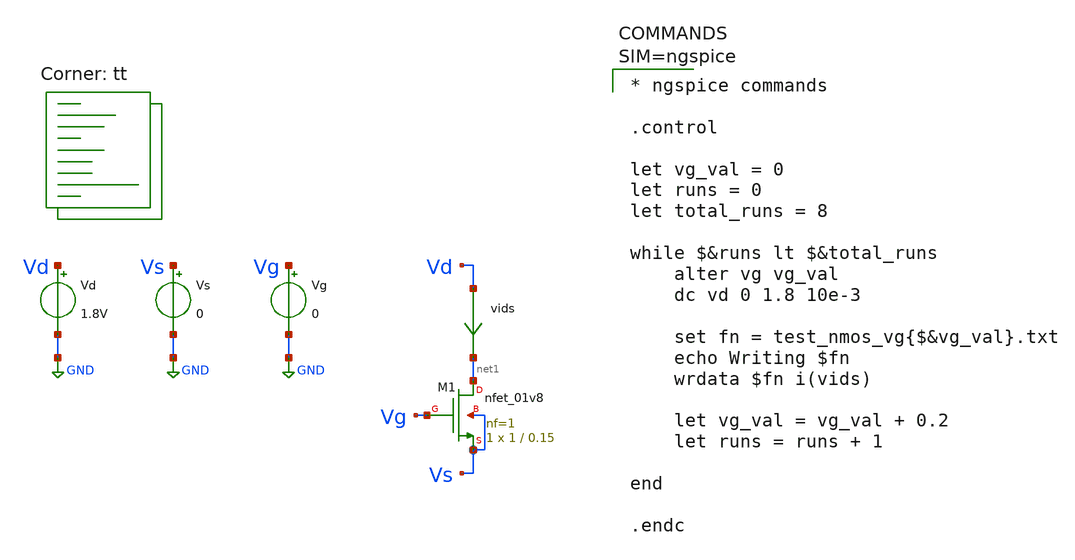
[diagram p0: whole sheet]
** sch_path: xschem/tests/dummy_tests/mos_meas_stepped_test.sch
**.subckt mos_meas_stepped_test
Vd Vd GND 1.8V
Vs Vs GND 0
XM1 net1 Vg Vs Vs sky130_fd_pr__nfet_01v8 L=0.15 W=1 nf=1 ad='int((nf+1)/2) * W/nf * 0.29' as='int((nf+2)/2) * W/nf * 0.29'
+ pd='2*int((nf+1)/2) * (W/nf + 0.29)' ps='2*int((nf+2)/2) * (W/nf + 0.29)' nrd='0.29 / W' nrs='0.29 / W'
+ sa=0 sb=0 sd=0 mult=1 m=1
vids Vd net1 0
.save i(vids)
Vg Vg GND 0
**** begin user architecture code
 *.lib $::SKYWATER_MODELS/sky130.lib.spice tt
.include $::SKYWATER_STDCELLS/sky130_fd_sc_hd.spice

.lib $::SKYWATER_MODELS/sky130.lib.spice tt


* ngspice commands

.control

let vg_val = 0
let runs = 0
let total_runs = 8

while $&runs lt $&total_runs
	alter vg vg_val
	dc vd 0 1.8 10e-3

	set fn = test_nmos_vg{$&vg_val}.txt
	echo Writing $fn
	wrdata $fn i(vids)

	let vg_val = vg_val + 0.2
	let runs = runs + 1

end

.endc







**** end user architecture code
**.ends
.GLOBAL GND
.end
